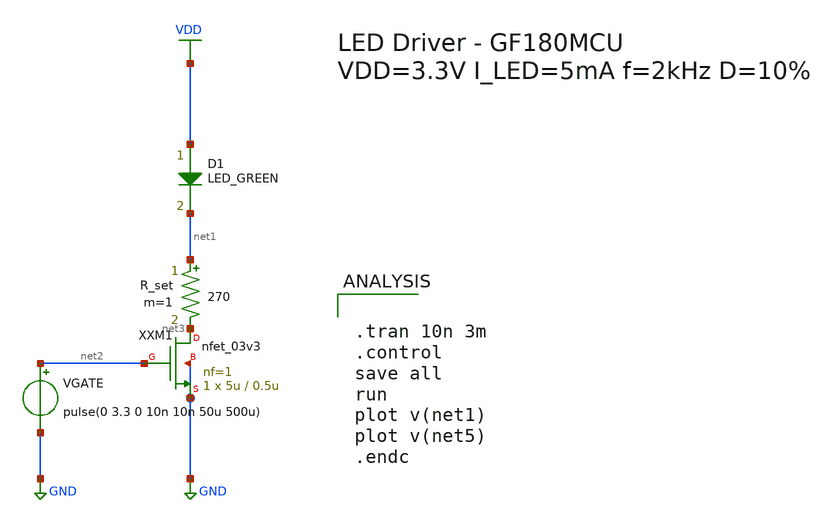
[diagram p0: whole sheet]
** sch_path: ps-led-driver/led_driver.sch
**.subckt led_driver
VGATE net2 GND pulse(0 3.3 0 10n 10n 50u 500u)
D1 VDD net1 LED_GREEN area=1e-6
R_set net1 net3 270 m=1
XXM1 net3 net2 GND GND nfet_03v3 L=0.5u W=5u nf=1 ad='int((nf+1)/2) * W/nf * 0.18u' as='int((nf+2)/2) * W/nf * 0.18u'
+ pd='2*int((nf+1)/2) * (W/nf + 0.18u)' ps='2*int((nf+2)/2) * (W/nf + 0.18u)' nrd='0.18u / W' nrs='0.18u / W'
+ sa=0 sb=0 sd=0 m=1
**** begin user architecture code


.include /foss/pdks/gf180mcuD/libs.tech/ngspice/design.ngspice
.lib /foss/pdks/gf180mcuD/libs.tech/ngspice/sm141064.ngspice typical
.model LED_GREEN D(Is=1e-20 N=2.0 Rs=5 Vj=2.1 Cjo=10p Tt=5n)
.ic V(VDD)=3.3




.tran 10n 3m
.control
save all
run
plot v(net1)
plot v(net5)
.endc


**** end user architecture code
**.ends
.GLOBAL VDD
.GLOBAL GND
.end
